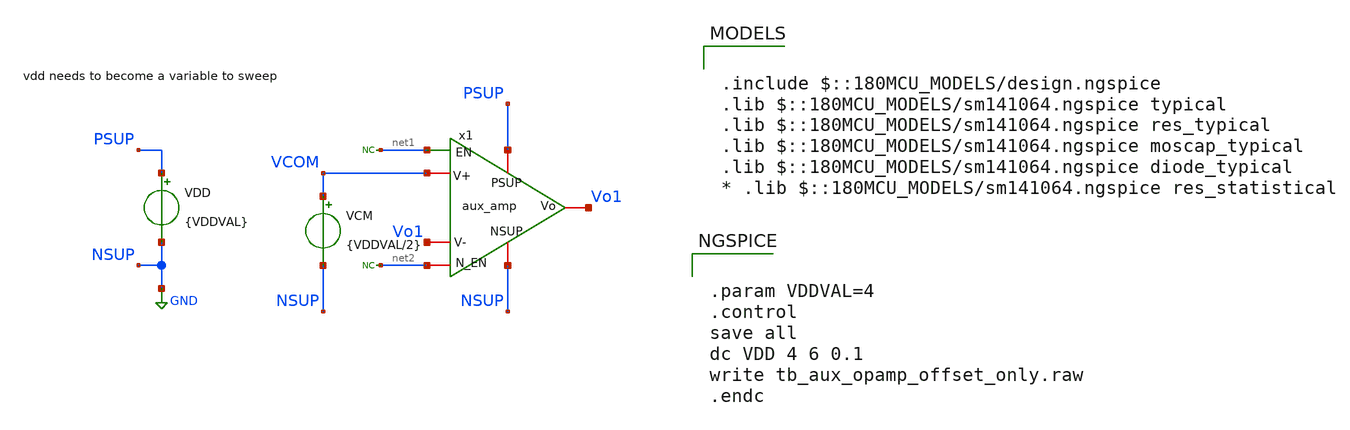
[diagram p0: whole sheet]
** sch_path: xschem/tb/tb_aux_opamp_offset_only.sch
**.subckt tb_aux_opamp_offset_only
* noconn #net1
* noconn #net2
x1 PSUP Vo1 VCOM Vo1 net2 NSUP net1 aux_amp
VDD PSUP NSUP {VDDVAL}
VCM VCOM NSUP {VDDVAL/2}
**** begin user architecture code

.include $::180MCU_MODELS/design.ngspice
.lib $::180MCU_MODELS/sm141064.ngspice typical
.lib $::180MCU_MODELS/sm141064.ngspice res_typical
.lib $::180MCU_MODELS/sm141064.ngspice moscap_typical
.lib $::180MCU_MODELS/sm141064.ngspice diode_typical
* .lib $::180MCU_MODELS/sm141064.ngspice res_statistical



.param VDDVAL=4
.control
save all
dc VDD 4 6 0.1
write tb_aux_opamp_offset_only.raw
.endc


**** end user architecture code
**.ends

* expanding   symbol:  lib/aux_amp.sym # of pins=7
** sym_path: xschem/lib/aux_amp.sym
** sch_path: xschem/lib/aux_amp.sch
.subckt aux_amp PSUP Vo V+ V- N_EN NSUP EN
*.ipin PSUP
*.ipin NSUP
*.ipin N_EN
*.ipin EN
*.ipin V+
*.ipin V-
*.opin Vo
XM1 Vo V- net2 net2 nfet_06v0 L=1.80u W=0.80u nf=1 ad='int((nf+1)/2) * W/nf * 0.18u' as='int((nf+2)/2) * W/nf * 0.18u'
+ pd='2*int((nf+1)/2) * (W/nf + 0.18u)' ps='2*int((nf+2)/2) * (W/nf + 0.18u)' nrd='0.18u / W' nrs='0.18u / W'
+ sa=0 sb=0 sd=0 m=1
XM2 net1 V+ net2 net2 nfet_06v0 L=1.80u W=0.80u nf=1 ad='int((nf+1)/2) * W/nf * 0.18u' as='int((nf+2)/2) * W/nf * 0.18u'
+ pd='2*int((nf+1)/2) * (W/nf + 0.18u)' ps='2*int((nf+2)/2) * (W/nf + 0.18u)' nrd='0.18u / W' nrs='0.18u / W'
+ sa=0 sb=0 sd=0 m=1
XM5 net1 net1 PSUP PSUP pfet_06v0 L=0.55u W=0.30u nf=1 ad='int((nf+1)/2) * W/nf * 0.18u' as='int((nf+2)/2) * W/nf * 0.18u'
+ pd='2*int((nf+1)/2) * (W/nf + 0.18u)' ps='2*int((nf+2)/2) * (W/nf + 0.18u)' nrd='0.18u / W' nrs='0.18u / W'
+ sa=0 sb=0 sd=0 m=1
XM6 Vo net1 PSUP PSUP pfet_06v0 L=0.55u W=0.30u nf=1 ad='int((nf+1)/2) * W/nf * 0.18u' as='int((nf+2)/2) * W/nf * 0.18u'
+ pd='2*int((nf+1)/2) * (W/nf + 0.18u)' ps='2*int((nf+2)/2) * (W/nf + 0.18u)' nrd='0.18u / W' nrs='0.18u / W'
+ sa=0 sb=0 sd=0 m=1
I0 net2 NSUP 5u
* noconn N_EN
* noconn EN
.ends

.GLOBAL GND
.end
